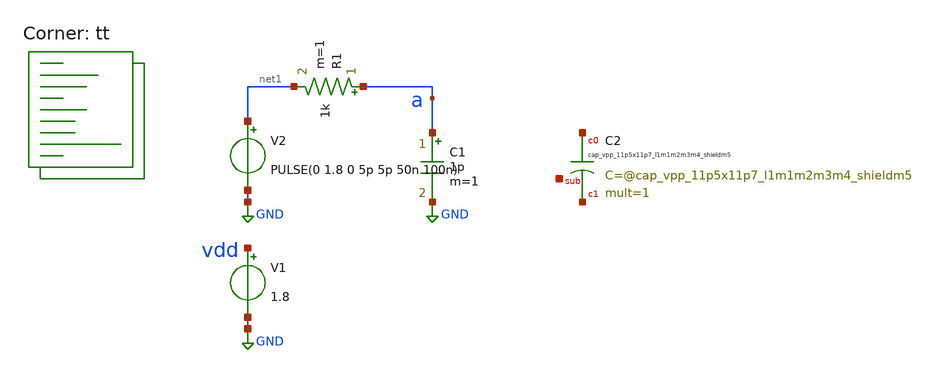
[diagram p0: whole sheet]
** sch_path: hgu/tb/tb_hgu_cdac_unit.sch
**.subckt tb_hgu_cdac_unit
V2 net1 GND PULSE(0 1.8 0 5p 5p 50n 100n)
R1 a net1 1k m=1
V1 vdd GND 1.8
C1 a GND 1p m=1
XC2 net2 net3 net4 sky130_fd_pr__cap_vpp_11p5x11p7_l1m1m2m3m4_shieldm5 mult=1 m=1
**** begin user architecture code


.save all
.temp = 100
.tran 100p 400n
.OPTIONS savecurrent
.include /foss/pdks/sky130A/libs.ref/sky130_fd_sc_hd/spice/sky130_fd_sc_hd.spice
.control
	run
        plot v(input) V(Q)
	let svdd = 1.62
	let max = svdd*0.8
	let min = svdd*0.2
	let mid = svdd*0.5
	meas tran rising_s find time when V(Q)=min RISE=1 TD=1000p
        meas tran rising_e find time when V(Q)=max RISE=1 TD=1000p
        let rising_time = rising_e-rising_s
        meas tran falling_s find time when V(Q)=max FALL=1 TD=1000p
        meas tran falling_e find time when V(Q)=min FALL=1 TD=1000p
        let falling_time = falling_e-falling_s
        meas tran IN find time when V(input)=mid RISE=1 TD=1000p
        meas tran OUT find time when V(Q)=mid RISE=1 TD=1000p
        let rising_delay = OUT-IN
	meas tran fIN find time when V(input)=mid FALL=1 TD=1000p
        meas tran fOUT find time when V(Q)=mid FALL=1 TD=1000p
        let falling_delay = fOUT-fIN

        print rising_time falling_time rising_delay falling_delay

.endc


.lib $::SKYWATER_MODELS/sky130.lib.spice tt
**** end user architecture code
**.ends
.GLOBAL GND
.end
